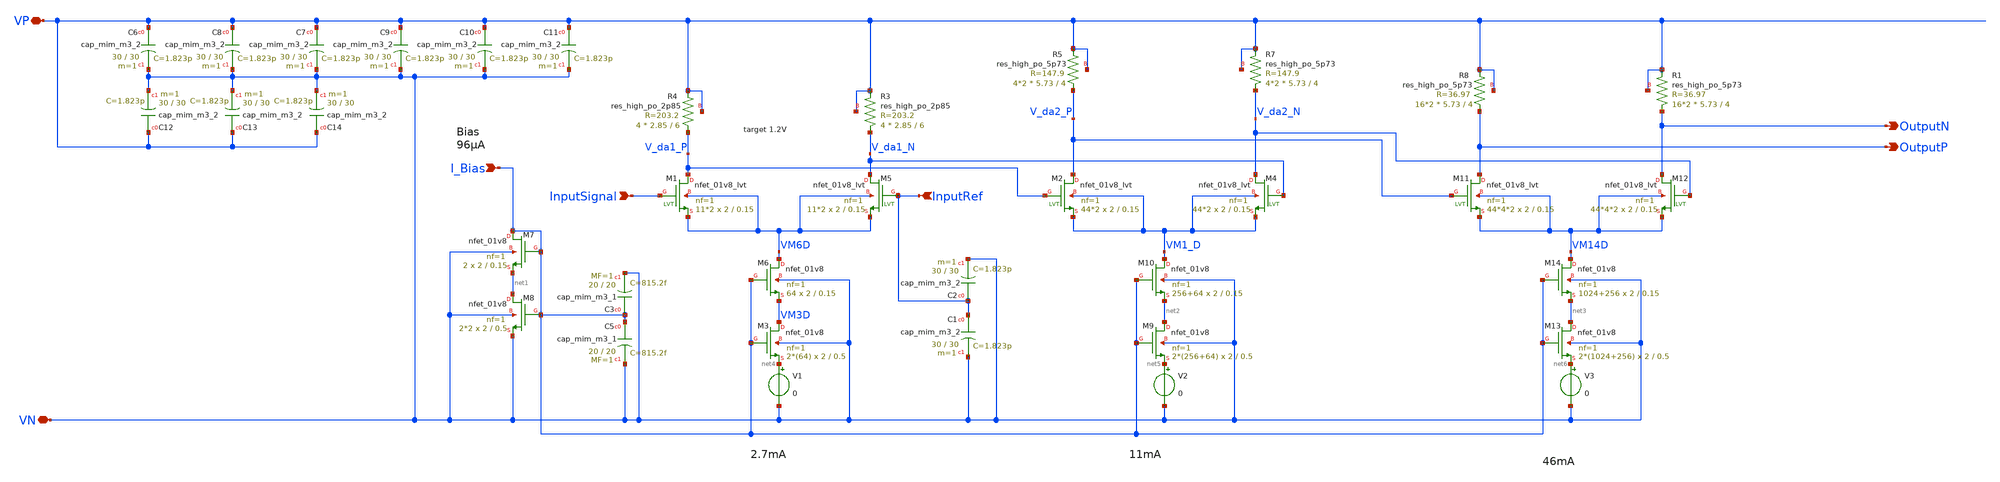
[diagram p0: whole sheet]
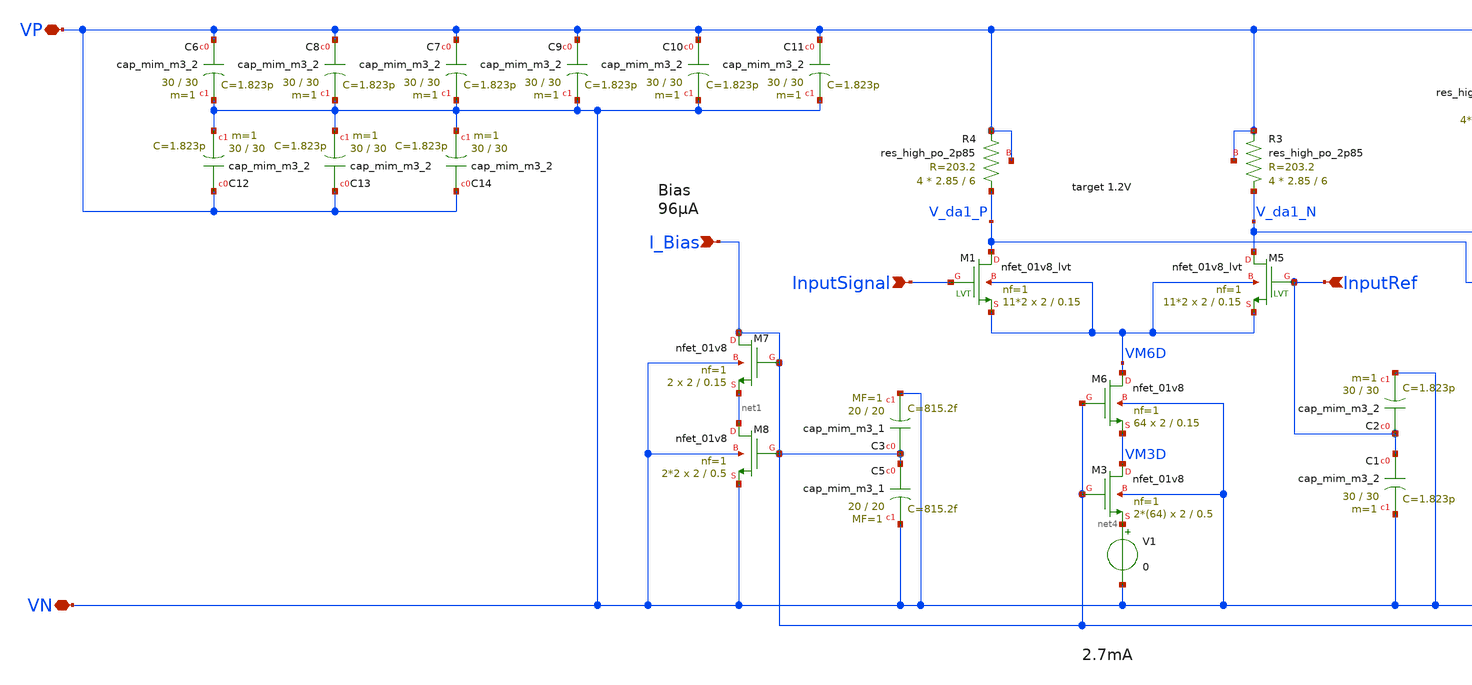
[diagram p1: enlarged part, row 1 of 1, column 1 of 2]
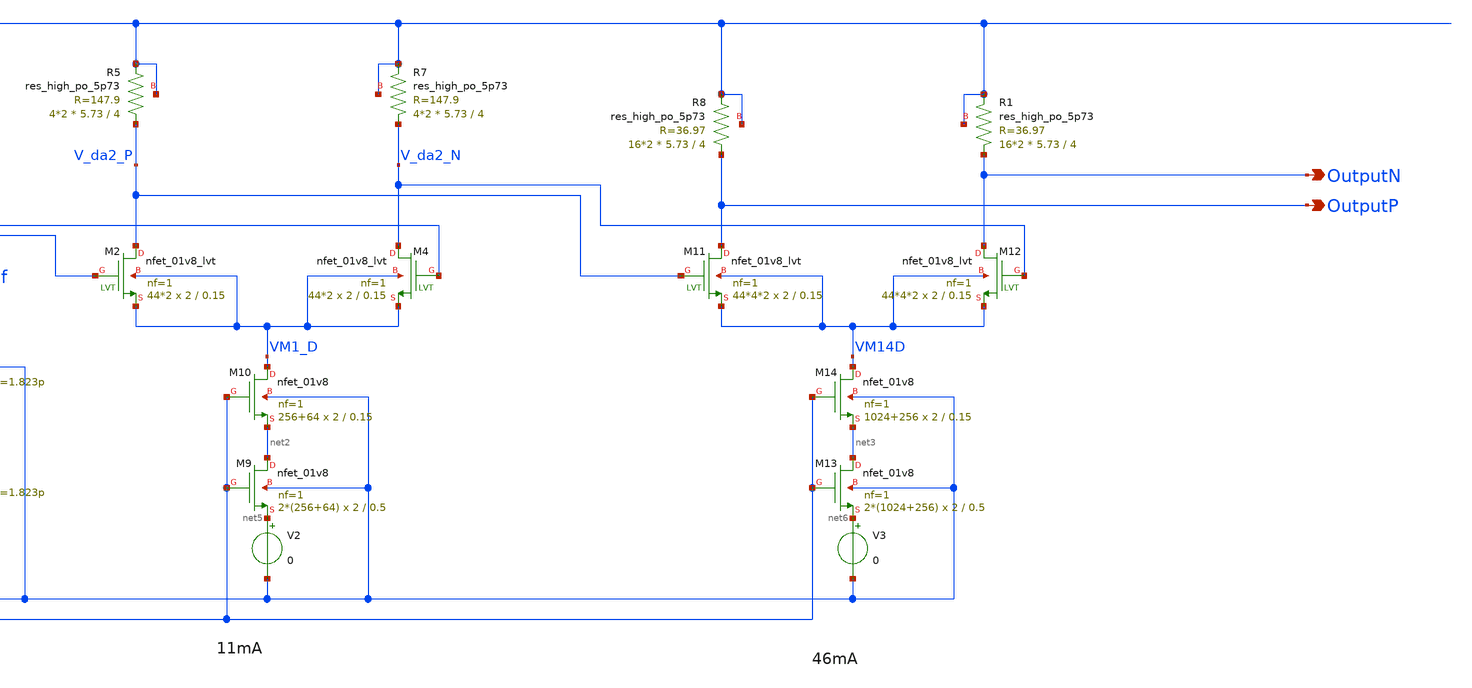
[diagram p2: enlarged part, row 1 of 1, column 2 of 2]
** sch_path: xschem/outdriver/outdriver.sch
**.subckt outdriver VN InputRef VP I_Bias InputSignal OutputN OutputP
*.iopin VN
*.ipin InputRef
*.iopin VP
*.ipin I_Bias
*.ipin InputSignal
*.opin OutputN
*.opin OutputP
XM1 V_da1_P InputSignal VM6D VM6D sky130_fd_pr__nfet_01v8_lvt L=0.15 W=2 nf=1 ad='int((nf+1)/2) * W/nf * 0.29'
+ as='int((nf+2)/2) * W/nf * 0.29' pd='2*int((nf+1)/2) * (W/nf + 0.29)' ps='2*int((nf+2)/2) * (W/nf + 0.29)'
+ nrd='0.29 / W' nrs='0.29 / W' sa=0 sb=0 sd=0 mult=11*2 m=11*2
XM3 VM3D I_Bias net4 VN sky130_fd_pr__nfet_01v8 L=0.5 W=2 nf=1 ad='int((nf+1)/2) * W/nf * 0.29' as='int((nf+2)/2) * W/nf * 0.29'
+ pd='2*int((nf+1)/2) * (W/nf + 0.29)' ps='2*int((nf+2)/2) * (W/nf + 0.29)' nrd='0.29 / W' nrs='0.29 / W'
+ sa=0 sb=0 sd=0 mult=2*(64) m=2*(64)
XM6 VM6D I_Bias VM3D VN sky130_fd_pr__nfet_01v8 L=0.15 W=2 nf=1 ad='int((nf+1)/2) * W/nf * 0.29' as='int((nf+2)/2) * W/nf * 0.29'
+ pd='2*int((nf+1)/2) * (W/nf + 0.29)' ps='2*int((nf+2)/2) * (W/nf + 0.29)' nrd='0.29 / W' nrs='0.29 / W'
+ sa=0 sb=0 sd=0 mult=64 m=64
XM7 I_Bias I_Bias net1 VN sky130_fd_pr__nfet_01v8 L=0.15 W=2 nf=1 ad='int((nf+1)/2) * W/nf * 0.29' as='int((nf+2)/2) * W/nf * 0.29'
+ pd='2*int((nf+1)/2) * (W/nf + 0.29)' ps='2*int((nf+2)/2) * (W/nf + 0.29)' nrd='0.29 / W' nrs='0.29 / W'
+ sa=0 sb=0 sd=0 mult=2 m=2
XM8 net1 I_Bias VN VN sky130_fd_pr__nfet_01v8 L=0.5 W=2 nf=1 ad='int((nf+1)/2) * W/nf * 0.29' as='int((nf+2)/2) * W/nf * 0.29'
+ pd='2*int((nf+1)/2) * (W/nf + 0.29)' ps='2*int((nf+2)/2) * (W/nf + 0.29)' nrd='0.29 / W' nrs='0.29 / W'
+ sa=0 sb=0 sd=0 mult=2*2 m=2*2
XM2 V_da2_P V_da1_P VM1_D VM1_D sky130_fd_pr__nfet_01v8_lvt L=0.15 W=2 nf=1 ad='int((nf+1)/2) * W/nf * 0.29'
+ as='int((nf+2)/2) * W/nf * 0.29' pd='2*int((nf+1)/2) * (W/nf + 0.29)' ps='2*int((nf+2)/2) * (W/nf + 0.29)'
+ nrd='0.29 / W' nrs='0.29 / W' sa=0 sb=0 sd=0 mult=44*2 m=44*2
XM4 V_da2_N V_da1_N VM1_D VM1_D sky130_fd_pr__nfet_01v8_lvt L=0.15 W=2 nf=1 ad='int((nf+1)/2) * W/nf * 0.29'
+ as='int((nf+2)/2) * W/nf * 0.29' pd='2*int((nf+1)/2) * (W/nf + 0.29)' ps='2*int((nf+2)/2) * (W/nf + 0.29)'
+ nrd='0.29 / W' nrs='0.29 / W' sa=0 sb=0 sd=0 mult=44*2 m=44*2
XM9 net2 I_Bias net5 VN sky130_fd_pr__nfet_01v8 L=0.5 W=2 nf=1 ad='int((nf+1)/2) * W/nf * 0.29' as='int((nf+2)/2) * W/nf * 0.29'
+ pd='2*int((nf+1)/2) * (W/nf + 0.29)' ps='2*int((nf+2)/2) * (W/nf + 0.29)' nrd='0.29 / W' nrs='0.29 / W'
+ sa=0 sb=0 sd=0 mult=2*(256+64) m=2*(256+64)
XM10 VM1_D I_Bias net2 VN sky130_fd_pr__nfet_01v8 L=0.15 W=2 nf=1 ad='int((nf+1)/2) * W/nf * 0.29' as='int((nf+2)/2) * W/nf * 0.29'
+ pd='2*int((nf+1)/2) * (W/nf + 0.29)' ps='2*int((nf+2)/2) * (W/nf + 0.29)' nrd='0.29 / W' nrs='0.29 / W'
+ sa=0 sb=0 sd=0 mult=256+64 m=256+64
XM11 OutputP V_da2_P VM14D VM14D sky130_fd_pr__nfet_01v8_lvt L=0.15 W=2 nf=1 ad='int((nf+1)/2) * W/nf * 0.29'
+ as='int((nf+2)/2) * W/nf * 0.29' pd='2*int((nf+1)/2) * (W/nf + 0.29)' ps='2*int((nf+2)/2) * (W/nf + 0.29)'
+ nrd='0.29 / W' nrs='0.29 / W' sa=0 sb=0 sd=0 mult=44*4*2 m=44*4*2
XM12 OutputN V_da2_N VM14D VM14D sky130_fd_pr__nfet_01v8_lvt L=0.15 W=2 nf=1 ad='int((nf+1)/2) * W/nf * 0.29'
+ as='int((nf+2)/2) * W/nf * 0.29' pd='2*int((nf+1)/2) * (W/nf + 0.29)' ps='2*int((nf+2)/2) * (W/nf + 0.29)'
+ nrd='0.29 / W' nrs='0.29 / W' sa=0 sb=0 sd=0 mult=44*4*2 m=44*4*2
XM13 net3 I_Bias net6 VN sky130_fd_pr__nfet_01v8 L=0.5 W=2 nf=1 ad='int((nf+1)/2) * W/nf * 0.29' as='int((nf+2)/2) * W/nf * 0.29'
+ pd='2*int((nf+1)/2) * (W/nf + 0.29)' ps='2*int((nf+2)/2) * (W/nf + 0.29)' nrd='0.29 / W' nrs='0.29 / W'
+ sa=0 sb=0 sd=0 mult=2*(1024+256) m=2*(1024+256)
XM14 VM14D I_Bias net3 VN sky130_fd_pr__nfet_01v8 L=0.15 W=2 nf=1 ad='int((nf+1)/2) * W/nf * 0.29' as='int((nf+2)/2) * W/nf * 0.29'
+ pd='2*int((nf+1)/2) * (W/nf + 0.29)' ps='2*int((nf+2)/2) * (W/nf + 0.29)' nrd='0.29 / W' nrs='0.29 / W'
+ sa=0 sb=0 sd=0 mult=1024+256 m=1024+256
XR7 V_da2_N VP VP sky130_fd_pr__res_high_po_5p73 L=4 mult=4*2 m=4*2
XR5 V_da2_P VP VP sky130_fd_pr__res_high_po_5p73 L=4 mult=4*2 m=4*2
XR3 V_da1_N VP VP sky130_fd_pr__res_high_po_2p85 L=6 mult=4 m=4
XR4 V_da1_P VP VP sky130_fd_pr__res_high_po_2p85 L=6 mult=4 m=4
XC2 InputRef VN sky130_fd_pr__cap_mim_m3_2 W=30 L=30 MF=1 m=1
XM5 V_da1_N InputRef VM6D VM6D sky130_fd_pr__nfet_01v8_lvt L=0.15 W=2 nf=1 ad='int((nf+1)/2) * W/nf * 0.29'
+ as='int((nf+2)/2) * W/nf * 0.29' pd='2*int((nf+1)/2) * (W/nf + 0.29)' ps='2*int((nf+2)/2) * (W/nf + 0.29)'
+ nrd='0.29 / W' nrs='0.29 / W' sa=0 sb=0 sd=0 mult=11*2 m=11*2
XR8 OutputP VP VP sky130_fd_pr__res_high_po_5p73 L=4 mult=16*2 m=16*2
XC1 InputRef VN sky130_fd_pr__cap_mim_m3_2 W=30 L=30 MF=1 m=1
XC6 VP VN sky130_fd_pr__cap_mim_m3_2 W=30 L=30 MF=1 m=1
XC8 VP VN sky130_fd_pr__cap_mim_m3_2 W=30 L=30 MF=1 m=1
V1 net4 VN 0
V2 net5 VN 0
V3 net6 VN 0
XR1 OutputN VP VP sky130_fd_pr__res_high_po_5p73 L=4 mult=16*2 m=16*2
XC7 VP VN sky130_fd_pr__cap_mim_m3_2 W=30 L=30 MF=1 m=1
XC9 VP VN sky130_fd_pr__cap_mim_m3_2 W=30 L=30 MF=1 m=1
XC10 VP VN sky130_fd_pr__cap_mim_m3_2 W=30 L=30 MF=1 m=1
XC11 VP VN sky130_fd_pr__cap_mim_m3_2 W=30 L=30 MF=1 m=1
XC12 VP VN sky130_fd_pr__cap_mim_m3_2 W=30 L=30 MF=1 m=1
XC13 VP VN sky130_fd_pr__cap_mim_m3_2 W=30 L=30 MF=1 m=1
XC14 VP VN sky130_fd_pr__cap_mim_m3_2 W=30 L=30 MF=1 m=1
XC5 I_Bias VN sky130_fd_pr__cap_mim_m3_1 W=20 L=20 MF=1 m=1
XC3 I_Bias VN sky130_fd_pr__cap_mim_m3_1 W=20 L=20 MF=1 m=1
**.ends
.end
